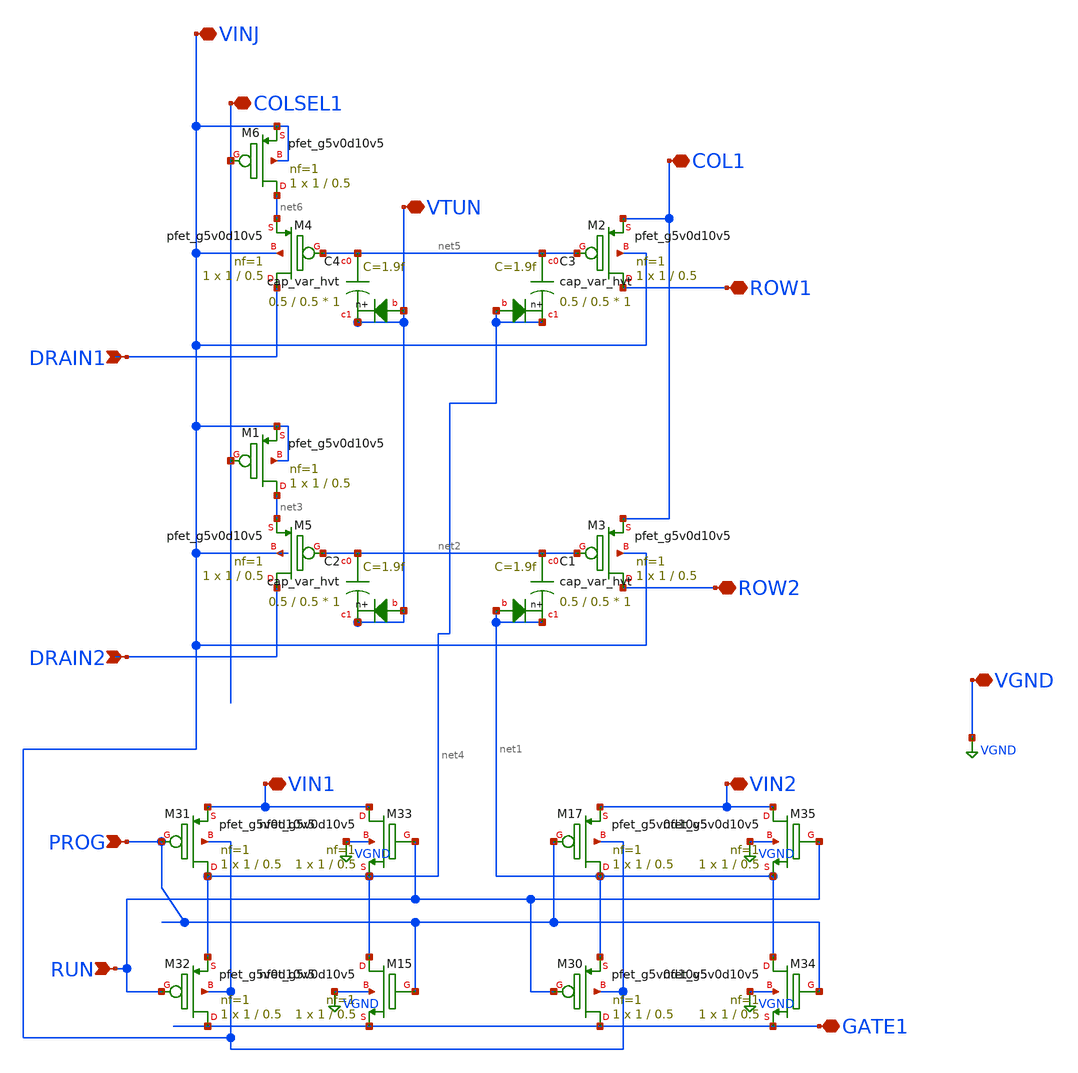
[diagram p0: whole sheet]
** sch_path: libs.ref/sky130_hilas_sc/xschem/sky130_hilas_FGtrans2x1cell.sch
**.subckt sky130_hilas_FGtrans2x1cell DRAIN1 DRAIN2 RUN PROG VTUN COLSEL1 VINJ GATE1 VIN1 VIN2 COL1
*+ ROW2 ROW1 VGND
*.ipin DRAIN1
*.ipin DRAIN2
*.ipin RUN
*.ipin PROG
*.iopin VTUN
*.iopin COLSEL1
*.iopin VINJ
*.iopin GATE1
*.iopin VIN1
*.iopin VIN2
*.iopin COL1
*.iopin ROW2
*.iopin ROW1
*.iopin VGND
XM3 ROW2 net2 COL1 VINJ sky130_fd_pr__pfet_g5v0d10v5 L=0.5 W=1 nf=1 ad='int((nf+1)/2) * W/nf * 0.29'
+ as='int((nf+2)/2) * W/nf * 0.29' pd='2*int((nf+1)/2) * (W/nf + 0.29)' ps='2*int((nf+2)/2) * (W/nf + 0.29)'
+ nrd='0.29 / W' nrs='0.29 / W' sa=0 sb=0 sd=0 mult=1 m=1
XC1 net2 net1 net1 sky130_fd_pr__cap_var_hvt W=0.5 L=0.5 VM=1 m=1
XM5 DRAIN2 net2 net3 VINJ sky130_fd_pr__pfet_g5v0d10v5 L=0.5 W=1 nf=1 ad='int((nf+1)/2) * W/nf * 0.29'
+ as='int((nf+2)/2) * W/nf * 0.29' pd='2*int((nf+1)/2) * (W/nf + 0.29)' ps='2*int((nf+2)/2) * (W/nf + 0.29)'
+ nrd='0.29 / W' nrs='0.29 / W' sa=0 sb=0 sd=0 mult=1 m=1
XC2 net2 VTUN VTUN sky130_fd_pr__cap_var_hvt W=0.5 L=0.5 VM=1 m=1
XM1 net3 COLSEL1 VINJ VINJ sky130_fd_pr__pfet_g5v0d10v5 L=0.5 W=1 nf=1 ad='int((nf+1)/2) * W/nf * 0.29'
+ as='int((nf+2)/2) * W/nf * 0.29' pd='2*int((nf+1)/2) * (W/nf + 0.29)' ps='2*int((nf+2)/2) * (W/nf + 0.29)'
+ nrd='0.29 / W' nrs='0.29 / W' sa=0 sb=0 sd=0 mult=1 m=1
XM2 ROW1 net5 COL1 VINJ sky130_fd_pr__pfet_g5v0d10v5 L=0.5 W=1 nf=1 ad='int((nf+1)/2) * W/nf * 0.29'
+ as='int((nf+2)/2) * W/nf * 0.29' pd='2*int((nf+1)/2) * (W/nf + 0.29)' ps='2*int((nf+2)/2) * (W/nf + 0.29)'
+ nrd='0.29 / W' nrs='0.29 / W' sa=0 sb=0 sd=0 mult=1 m=1
XC3 net5 net4 net4 sky130_fd_pr__cap_var_hvt W=0.5 L=0.5 VM=1 m=1
XM4 DRAIN1 net5 net6 VINJ sky130_fd_pr__pfet_g5v0d10v5 L=0.5 W=1 nf=1 ad='int((nf+1)/2) * W/nf * 0.29'
+ as='int((nf+2)/2) * W/nf * 0.29' pd='2*int((nf+1)/2) * (W/nf + 0.29)' ps='2*int((nf+2)/2) * (W/nf + 0.29)'
+ nrd='0.29 / W' nrs='0.29 / W' sa=0 sb=0 sd=0 mult=1 m=1
XC4 net5 VTUN VTUN sky130_fd_pr__cap_var_hvt W=0.5 L=0.5 VM=1 m=1
XM6 net6 COLSEL1 VINJ VINJ sky130_fd_pr__pfet_g5v0d10v5 L=0.5 W=1 nf=1 ad='int((nf+1)/2) * W/nf * 0.29'
+ as='int((nf+2)/2) * W/nf * 0.29' pd='2*int((nf+1)/2) * (W/nf + 0.29)' ps='2*int((nf+2)/2) * (W/nf + 0.29)'
+ nrd='0.29 / W' nrs='0.29 / W' sa=0 sb=0 sd=0 mult=1 m=1
XM15 net4 PROG GATE1 VGND sky130_fd_pr__nfet_g5v0d10v5 L=0.5 W=1 nf=1 ad='int((nf+1)/2) * W/nf * 0.29'
+ as='int((nf+2)/2) * W/nf * 0.29' pd='2*int((nf+1)/2) * (W/nf + 0.29)' ps='2*int((nf+2)/2) * (W/nf + 0.29)'
+ nrd='0.29 / W' nrs='0.29 / W' sa=0 sb=0 sd=0 mult=1 m=1
XM17 net1 PROG VIN2 VINJ sky130_fd_pr__pfet_g5v0d10v5 L=0.5 W=1 nf=1 ad='int((nf+1)/2) * W/nf * 0.29'
+ as='int((nf+2)/2) * W/nf * 0.29' pd='2*int((nf+1)/2) * (W/nf + 0.29)' ps='2*int((nf+2)/2) * (W/nf + 0.29)'
+ nrd='0.29 / W' nrs='0.29 / W' sa=0 sb=0 sd=0 mult=1 m=1
XM30 GATE1 RUN net1 VINJ sky130_fd_pr__pfet_g5v0d10v5 L=0.5 W=1 nf=1 ad='int((nf+1)/2) * W/nf * 0.29'
+ as='int((nf+2)/2) * W/nf * 0.29' pd='2*int((nf+1)/2) * (W/nf + 0.29)' ps='2*int((nf+2)/2) * (W/nf + 0.29)'
+ nrd='0.29 / W' nrs='0.29 / W' sa=0 sb=0 sd=0 mult=1 m=1
XM31 net4 PROG VIN1 VINJ sky130_fd_pr__pfet_g5v0d10v5 L=0.5 W=1 nf=1 ad='int((nf+1)/2) * W/nf * 0.29'
+ as='int((nf+2)/2) * W/nf * 0.29' pd='2*int((nf+1)/2) * (W/nf + 0.29)' ps='2*int((nf+2)/2) * (W/nf + 0.29)'
+ nrd='0.29 / W' nrs='0.29 / W' sa=0 sb=0 sd=0 mult=1 m=1
XM32 GATE1 RUN net4 VINJ sky130_fd_pr__pfet_g5v0d10v5 L=0.5 W=1 nf=1 ad='int((nf+1)/2) * W/nf * 0.29'
+ as='int((nf+2)/2) * W/nf * 0.29' pd='2*int((nf+1)/2) * (W/nf + 0.29)' ps='2*int((nf+2)/2) * (W/nf + 0.29)'
+ nrd='0.29 / W' nrs='0.29 / W' sa=0 sb=0 sd=0 mult=1 m=1
XM33 VIN1 RUN net4 VGND sky130_fd_pr__nfet_g5v0d10v5 L=0.5 W=1 nf=1 ad='int((nf+1)/2) * W/nf * 0.29'
+ as='int((nf+2)/2) * W/nf * 0.29' pd='2*int((nf+1)/2) * (W/nf + 0.29)' ps='2*int((nf+2)/2) * (W/nf + 0.29)'
+ nrd='0.29 / W' nrs='0.29 / W' sa=0 sb=0 sd=0 mult=1 m=1
XM34 net1 PROG GATE1 VGND sky130_fd_pr__nfet_g5v0d10v5 L=0.5 W=1 nf=1 ad='int((nf+1)/2) * W/nf * 0.29'
+ as='int((nf+2)/2) * W/nf * 0.29' pd='2*int((nf+1)/2) * (W/nf + 0.29)' ps='2*int((nf+2)/2) * (W/nf + 0.29)'
+ nrd='0.29 / W' nrs='0.29 / W' sa=0 sb=0 sd=0 mult=1 m=1
XM35 VIN2 RUN net1 VGND sky130_fd_pr__nfet_g5v0d10v5 L=0.5 W=1 nf=1 ad='int((nf+1)/2) * W/nf * 0.29'
+ as='int((nf+2)/2) * W/nf * 0.29' pd='2*int((nf+1)/2) * (W/nf + 0.29)' ps='2*int((nf+2)/2) * (W/nf + 0.29)'
+ nrd='0.29 / W' nrs='0.29 / W' sa=0 sb=0 sd=0 mult=1 m=1
**.ends
.GLOBAL VGND
.end
